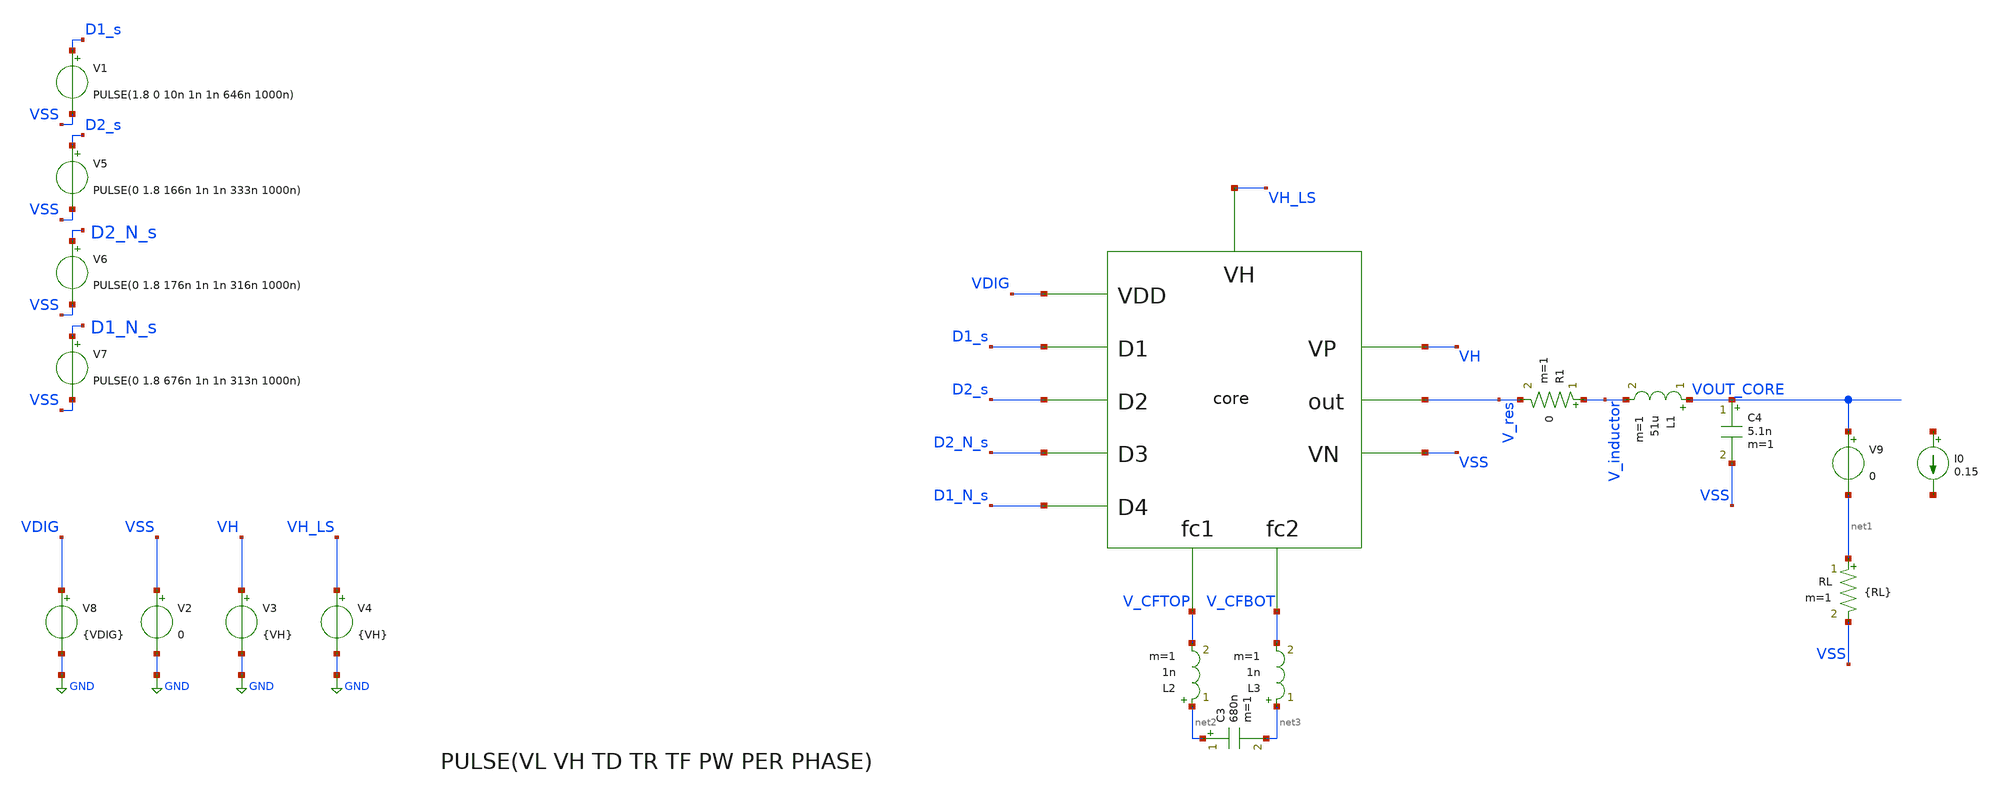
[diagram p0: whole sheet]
** sch_path: Notebooks/3LFCC/core_testbench_wfilter.sch
**.subckt core_testbench_wfilter
V2 VSS GND 0
V3 VH GND {VH}
I0 net4 net5 0.15
RL net1 VSS {RL} m=1
V8 VDIG GND {VDIG}
V6 D2_N_s VSS PULSE(0 1.8 176n 1n 1n 316n 1000n)
V5 D2_s VSS PULSE(0 1.8 166n 1n 1n 333n 1000n)
V7 D1_N_s VSS PULSE(0 1.8 676n 1n 1n 313n 1000n)
V1 D1_s VSS PULSE(1.8 0 10n 1n 1n 646n 1000n)
V4 VH_LS GND {VH}
V9 VOUT_CORE net1 0
C4 VOUT_CORE VSS 5.1n m=1
L1 VOUT_CORE V_inductor 51u m=1
R1 V_inductor V_res 0 m=1
X1 VDIG D2_s D1_s VH VSS V_res D2_N_s D1_N_s V_CFTOP V_CFBOT VH_LS core
C3 net2 net3 680n m=1
L2 net2 V_CFTOP 1n m=1
L3 net3 V_CFBOT 1n m=1
**** begin user architecture code


.param VIN = 5
.param VDIG = 1.8
.param VH = 5
.param RL = 50
.option scale=1e-6
*.option temp=70
.ic v(V_CFTOP) = VH/2
.ic v(vout_core)=3
.ic v(V_CFBOT) = 0
*.probe vd(MP2:G:S)
.save v(D1) v(D2) v(D1_N) v(D2_N) v(VOUT_CORE) v(vh) i(v9) i(v3) i(v4) v(v_cftop,v_cfbot) v(D1,v_cftop) v(D2,vout_core) v(D2_N,v_cfbot) v(D1_Nv,VSS) v(v_out_ls1) v(v_out_ls2) v(d2_n,v_cfbot) v(D1_s) v(D2_s)	v(D2_N_s) v(D1_N_s)
.save @m.xm4.msky130_fd_pr__nfet_g5v0d10v5[vds]
.param mc_mm_switch=0

.lib /foss/pdk/sky130A/libs.tech/ngspice/sky130.lib.spice TT

.options savecurrents


.control
compose resist values 300 44 22 11 (5.5) 3
foreach res $&resist
alterparam RL=$res
reset
tran 1n 30u
run
wrdata /foss/designs/personal/3LFCC_AC3E/xschem/testbench/Core/3LFCC_core_wfilter.txt
+ tran.v(vout_core) tran.i(v3) tran.i(v4) tran.i(v9)
set appendwrite
end

*Relación Pulso P y N para acondicionar tiempos muertos (reducir peaks)







**Problema actual, eficiencia no se logra calcular debido a que no transicionan bien todo los
*+ estados, (Cuando el Flycap esta flotante no esta consumiendo energía, es decir la carga no esta conectada a
*+ la fuente de entrada...)
** Si bien D1- D1_N y D2- D2_N estan con sus respectivos tiempos muertos (redución de peaks), falta
*+ sincronizar bien D1 con D2 para lograr la conexión correcta para que la carga se conecte a la fuente en estado
*+ de flycap flotante.

.endc


**** end user architecture code
**.ends
.GLOBAL GND
.end
